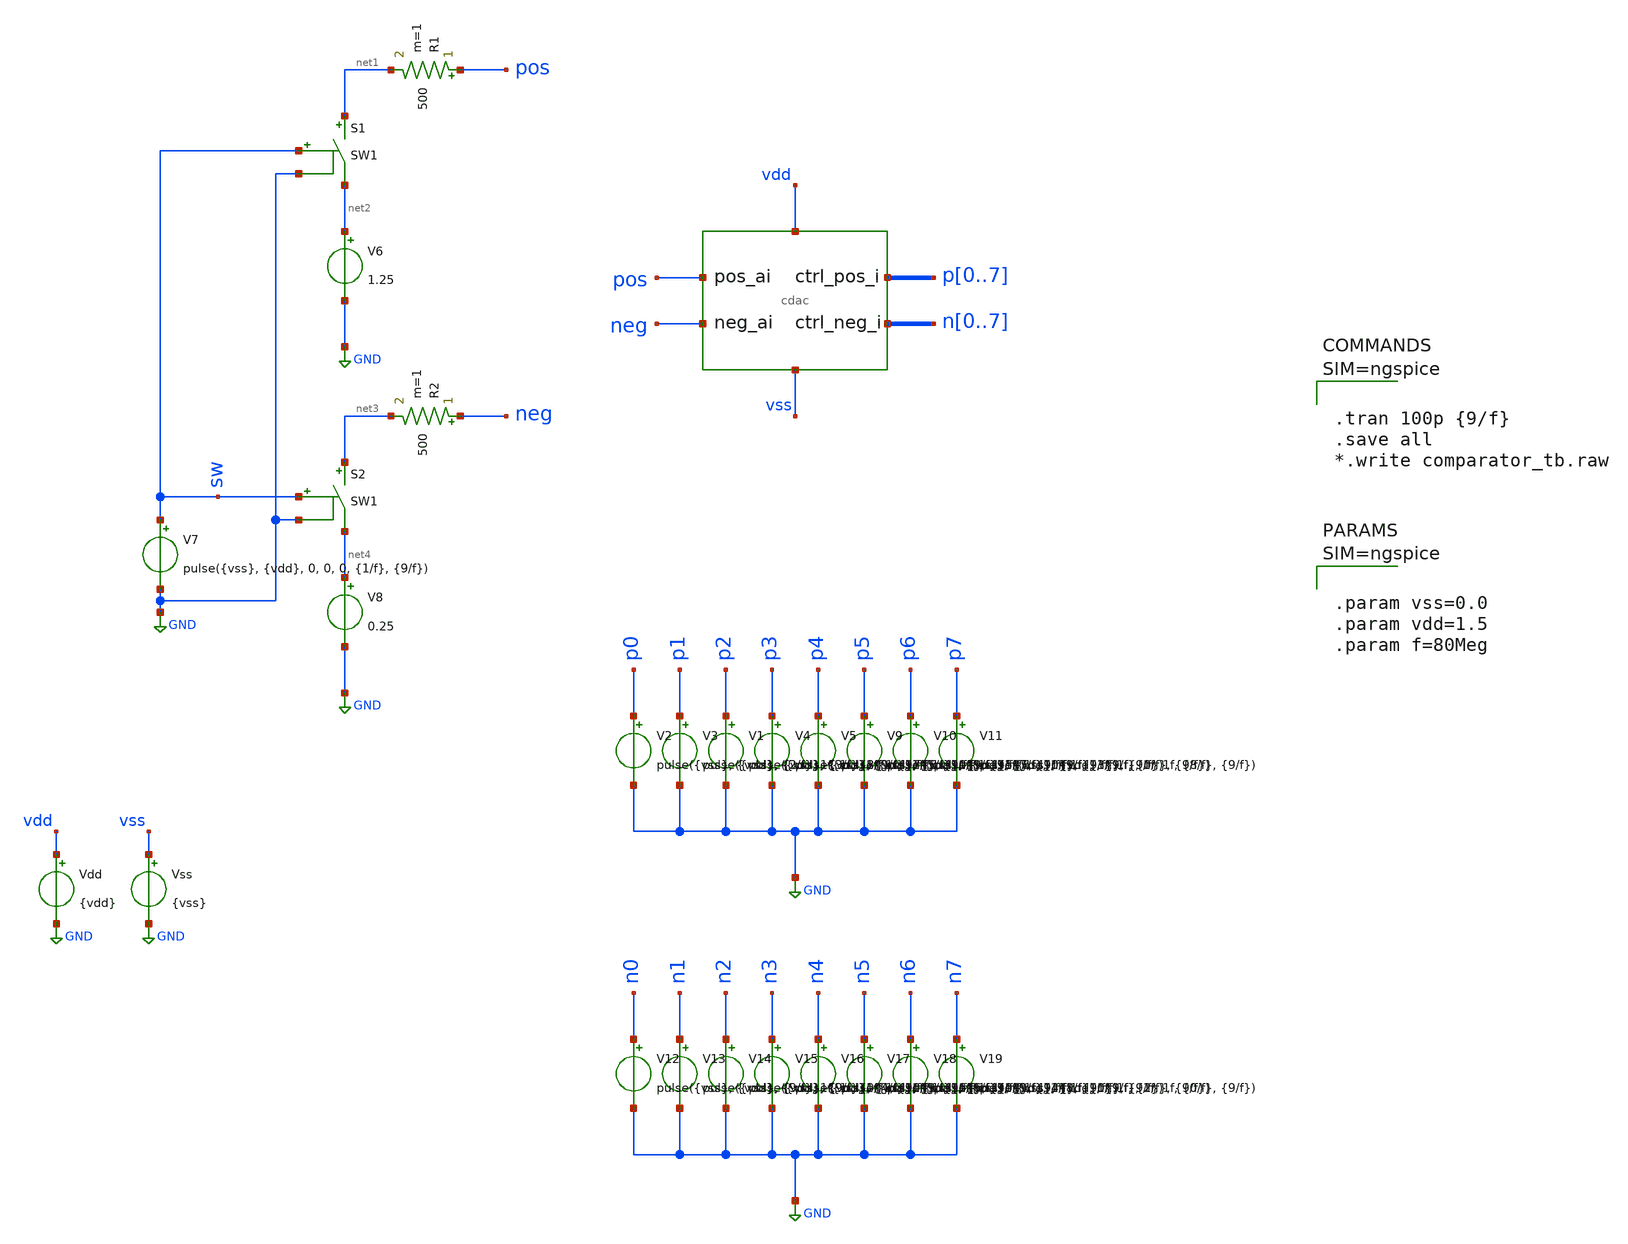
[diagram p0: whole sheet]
** sch_path: designs/cdac_diff/cdac_tb.sch
* IHP-GmbH/IHP-Open-PDK/ihp-sg13g2/libs.tech/xschem/sg13g2_stdcells/sg13g2_inv_2.sch:
* Copyright 2023 IHP PDK Authors
* Licensed under the Apache License, Version 2.0 (the "License");
**.subckt cdac_tb
x1 pos neg vss vdd p0 p1 p2 p3 p4 p5 p6 p7 n0 n1 n2 n3 n4 n5 n6 n7 cdac
S1 net1 net2 sw GND SW1
R1 pos net1 500 m=1
Vdd vdd GND {vdd}
Vss vss GND {vss}
V2 p0 GND pulse({vss}, {vdd}, {2/f}, 1f, 1f, {8/f}, {9/f})
V3 p1 GND pulse({vss}, {vdd}, {3/f}, 1f, 1f, {7/f}, {9/f})
V6 net2 GND 1.25
S2 net3 net4 sw GND SW1
R2 neg net3 500 m=1
V7 sw GND pulse({vss}, {vdd}, 0, 0, 0, {1/f}, {9/f})
V8 net4 GND 0.25
V1 p2 GND pulse({vss}, {vdd}, {9/f}, 1f, 1f, {0/f}, {9/f})
V4 p3 GND pulse({vss}, {vdd}, {5/f}, 1f, 1f, {5/f}, {9/f})
V5 p4 GND pulse({vss}, {vdd}, {9/f}, 1f, 1f, {0/f}, {9/f})
V9 p5 GND pulse({vss}, {vdd}, {7/f}, 1f, 1f, {3/f}, {9/f})
V10 p6 GND pulse({vss}, {vdd}, {9/f}, 1f, 1f, {0/f}, {9/f})
V11 p7 GND pulse({vss}, {vdd}, {9/f}, 1f, 1f, {8/f}, {9/f})
V12 n0 GND pulse({vss}, {vdd}, {9/f}, 1f, 1f, {0/f}, {9/f})
V13 n1 GND pulse({vss}, {vdd}, {9/f}, 1f, 1f, {0/f}, {9/f})
V14 n2 GND pulse({vss}, {vdd}, {4/f}, 1f, 1f, {6/f}, {9/f})
V15 n3 GND pulse({vss}, {vdd}, {9/f}, 1f, 1f, {0/f}, {9/f})
V16 n4 GND pulse({vss}, {vdd}, {6/f}, 1f, 1f, {4/f}, {9/f})
V17 n5 GND pulse({vss}, {vdd}, {9/f}, 1f, 1f, {0/f}, {9/f})
V18 n6 GND pulse({vss}, {vdd}, {8/f}, 1f, 1f, {2/f}, {9/f})
V19 n7 GND pulse({vss}, {vdd}, {9/f}, 1f, 1f, {0/f}, {9/f})
**** begin user architecture code

.lib $::SG13G2_MODELS/cornerMOSlv.lib mos_tt
.lib $::SG13G2_MODELS/cornerCAP.lib cap_typ
.include $::PDK_ROOT/ihp-sg13g2/libs.ref/sg13g2_stdcell/spice/sg13g2_stdcell.spice




.tran 100p {9/f}
.save all
*.write comparator_tb.raw






.param vss=0.0
.param vdd=1.5
.param f=80Meg



**** end user architecture code
**.ends

* expanding   symbol:  cdac.sym # of pins=6
** sym_path: designs/cdac_diff/cdac.sym
** sch_path: designs/cdac_diff/cdac.sch
.subckt cdac pos_ai neg_ai VSS VDD pos_ctrl_i0 pos_ctrl_i1 pos_ctrl_i2 pos_ctrl_i3 pos_ctrl_i4
+ pos_ctrl_i5 pos_ctrl_i6 pos_ctrl_i7 neg_ctrl_i0 neg_ctrl_i1 neg_ctrl_i2 neg_ctrl_i3 neg_ctrl_i4 neg_ctrl_i5
+ neg_ctrl_i6 neg_ctrl_i7
*.ipin pos_ai
*.ipin VSS
*.ipin VDD
*.ipin neg_ai
*.ipin
*+ pos_ctrl_i0,pos_ctrl_i1,pos_ctrl_i2,pos_ctrl_i3,pos_ctrl_i4,pos_ctrl_i5,pos_ctrl_i6,pos_ctrl_i7
*.ipin
*+ neg_ctrl_i0,neg_ctrl_i1,neg_ctrl_i2,neg_ctrl_i3,neg_ctrl_i4,neg_ctrl_i5,neg_ctrl_i6,neg_ctrl_i7
x1 net1 pos_ctrl_i0 VDD VSS sg13g2_inv_2
x2 net2 pos_ctrl_i1 VDD VSS sg13g2_inv_2
x3 net3 pos_ctrl_i2 VDD VSS sg13g2_inv_2
x4 net4 pos_ctrl_i3 VDD VSS sg13g2_inv_2
x5 net5 pos_ctrl_i4 VDD VSS sg13g2_inv_2
x6 net6 pos_ctrl_i5 VDD VSS sg13g2_inv_2
x7 net7 pos_ctrl_i6 VDD VSS sg13g2_inv_2
x8 net8 pos_ctrl_i7 VDD VSS sg13g2_inv_2
XC1 pos_ai net8 cap_cmim w=2.5292e-6 l=2.5292e-6 m=1 mm_ok=1
XC2 pos_ai net7 cap_cmim w=2.5292e-6 l=2.5292e-6 m=2 mm_ok=1
XC3 pos_ai net6 cap_cmim w=2.5292e-6 l=2.5292e-6 m=4 mm_ok=1
XC4 pos_ai net5 cap_cmim w=2.5292e-6 l=2.5292e-6 m=8 mm_ok=1
XC9 pos_ai VSS cap_cmim w=2.5292e-6 l=2.5292e-6 m=1 mm_ok=1
x9 net9 neg_ctrl_i0 VDD VSS sg13g2_inv_2
x10 net10 neg_ctrl_i1 VDD VSS sg13g2_inv_2
x11 net11 neg_ctrl_i2 VDD VSS sg13g2_inv_2
x12 net12 neg_ctrl_i3 VDD VSS sg13g2_inv_2
x13 net13 neg_ctrl_i4 VDD VSS sg13g2_inv_2
x14 net14 neg_ctrl_i5 VDD VSS sg13g2_inv_2
x15 net15 neg_ctrl_i6 VDD VSS sg13g2_inv_2
x16 net16 neg_ctrl_i7 VDD VSS sg13g2_inv_2
XC10 neg_ai net16 cap_cmim w=2.5292e-6 l=2.5292e-6 m=1 mm_ok=1
XC11 neg_ai net15 cap_cmim w=2.5292e-6 l=2.5292e-6 m=2 mm_ok=1
XC12 neg_ai net14 cap_cmim w=2.5292e-6 l=2.5292e-6 m=4 mm_ok=1
XC13 neg_ai net13 cap_cmim w=2.5292e-6 l=2.5292e-6 m=8 mm_ok=1
XC18 neg_ai VSS cap_cmim w=2.5292e-6 l=2.5292e-6 m=1 mm_ok=1
XC8 pos_ai net1 cap_cmim w=2.5292e-6 l=2.5292e-6 m=64 mm_ok=1
XC17 neg_ai net9 cap_cmim w=2.5292e-6 l=2.5292e-6 m=64 mm_ok=1
XC19 neg_ai net18 cap_cmim w=2.5292e-6 l=2.5292e-6 m=64 mm_ok=1
XC20 pos_ai net17 cap_cmim w=2.5292e-6 l=2.5292e-6 m=64 mm_ok=1
XC7 neg_ai net10 cap_cmim w=2.5292e-6 l=2.5292e-6 m=32 mm_ok=1
XC16 pos_ai net2 cap_cmim w=2.5292e-6 l=2.5292e-6 m=32 mm_ok=1
XC21 pos_ai net19 cap_cmim w=2.5292e-6 l=2.5292e-6 m=32 mm_ok=1
XC22 neg_ai net20 cap_cmim w=2.5292e-6 l=2.5292e-6 m=32 mm_ok=1
XC23 neg_ai net22 cap_cmim w=2.5292e-6 l=2.5292e-6 m=16 mm_ok=1
XC24 pos_ai net21 cap_cmim w=2.5292e-6 l=2.5292e-6 m=16 mm_ok=1
XC6 neg_ai net11 cap_cmim w=2.5292e-6 l=2.5292e-6 m=16 mm_ok=1
XC15 pos_ai net3 cap_cmim w=2.5292e-6 l=2.5292e-6 m=16 mm_ok=1
XC25 neg_ai net24 cap_cmim w=2.5292e-6 l=2.5292e-6 m=8 mm_ok=1
XC26 pos_ai net23 cap_cmim w=2.5292e-6 l=2.5292e-6 m=8 mm_ok=1
XC5 pos_ai net4 cap_cmim w=2.5292e-6 l=2.5292e-6 m=8 mm_ok=1
XC14 neg_ai net12 cap_cmim w=2.5292e-6 l=2.5292e-6 m=8 mm_ok=1
* noconn VDD
x17 net17 neg_ctrl_i0 VDD VSS sg13g2_buf_2
x21 net18 pos_ctrl_i0 VDD VSS sg13g2_buf_2
x18 net19 neg_ctrl_i1 VDD VSS sg13g2_buf_2
x19 net20 pos_ctrl_i1 VDD VSS sg13g2_buf_2
x20 net21 neg_ctrl_i2 VDD VSS sg13g2_buf_2
x22 net22 pos_ctrl_i2 VDD VSS sg13g2_buf_2
x23 net23 neg_ctrl_i3 VDD VSS sg13g2_buf_2
x24 net24 pos_ctrl_i3 VDD VSS sg13g2_buf_2
.ends


* expanding   symbol:  sg13g2_stdcells/sg13g2_inv_2.sym # of pins=2
** sym_path: sg13g2_stdcells/sg13g2_inv_2.sym
** sch_path: sg13g2_stdcells/sg13g2_inv_2.sch
.subckt sg13g2_inv_2 Y A VDD VSS
*.opin Y
*.ipin A
*.iopin VDD
*.iopin VSS
XM1 Y A VSS VSS sg13_lv_nmos w=1.48u l=130.00n ng=2 m=1 mm_ok=1
XM2 Y A VDD VDD sg13_lv_pmos w=2.24u l=130.00n ng=2 m=1 mm_ok=1
.ends


* expanding   symbol:  sg13g2_stdcells/sg13g2_buf_2.sym # of pins=2
** sym_path: sg13g2_stdcells/sg13g2_buf_2.sym
** sch_path: sg13g2_stdcells/sg13g2_buf_2.sch
.subckt sg13g2_buf_2 X A VDD VSS
*.ipin A
*.opin X
*.iopin VDD
*.iopin VSS
XM1 net1 A VSS VSS sg13_lv_nmos w=640.00n l=130.00n ng=1 m=1 mm_ok=1
XM2 X net1 VSS VSS sg13_lv_nmos w=1.48u l=130.00n ng=2 m=1 mm_ok=1
XM3 net1 A VDD VDD sg13_lv_pmos w=1.000u l=130.00n ng=1 m=1 mm_ok=1
XM4 X net1 VDD VDD sg13_lv_pmos w=2.24u l=130.00n ng=2 m=1 mm_ok=1
.ends

.GLOBAL GND
**** begin user architecture code
.MODEL SW1 SW   VT=0.9 VH=0.01  RON=0.01 ROFF=10G
**** end user architecture code
.end
